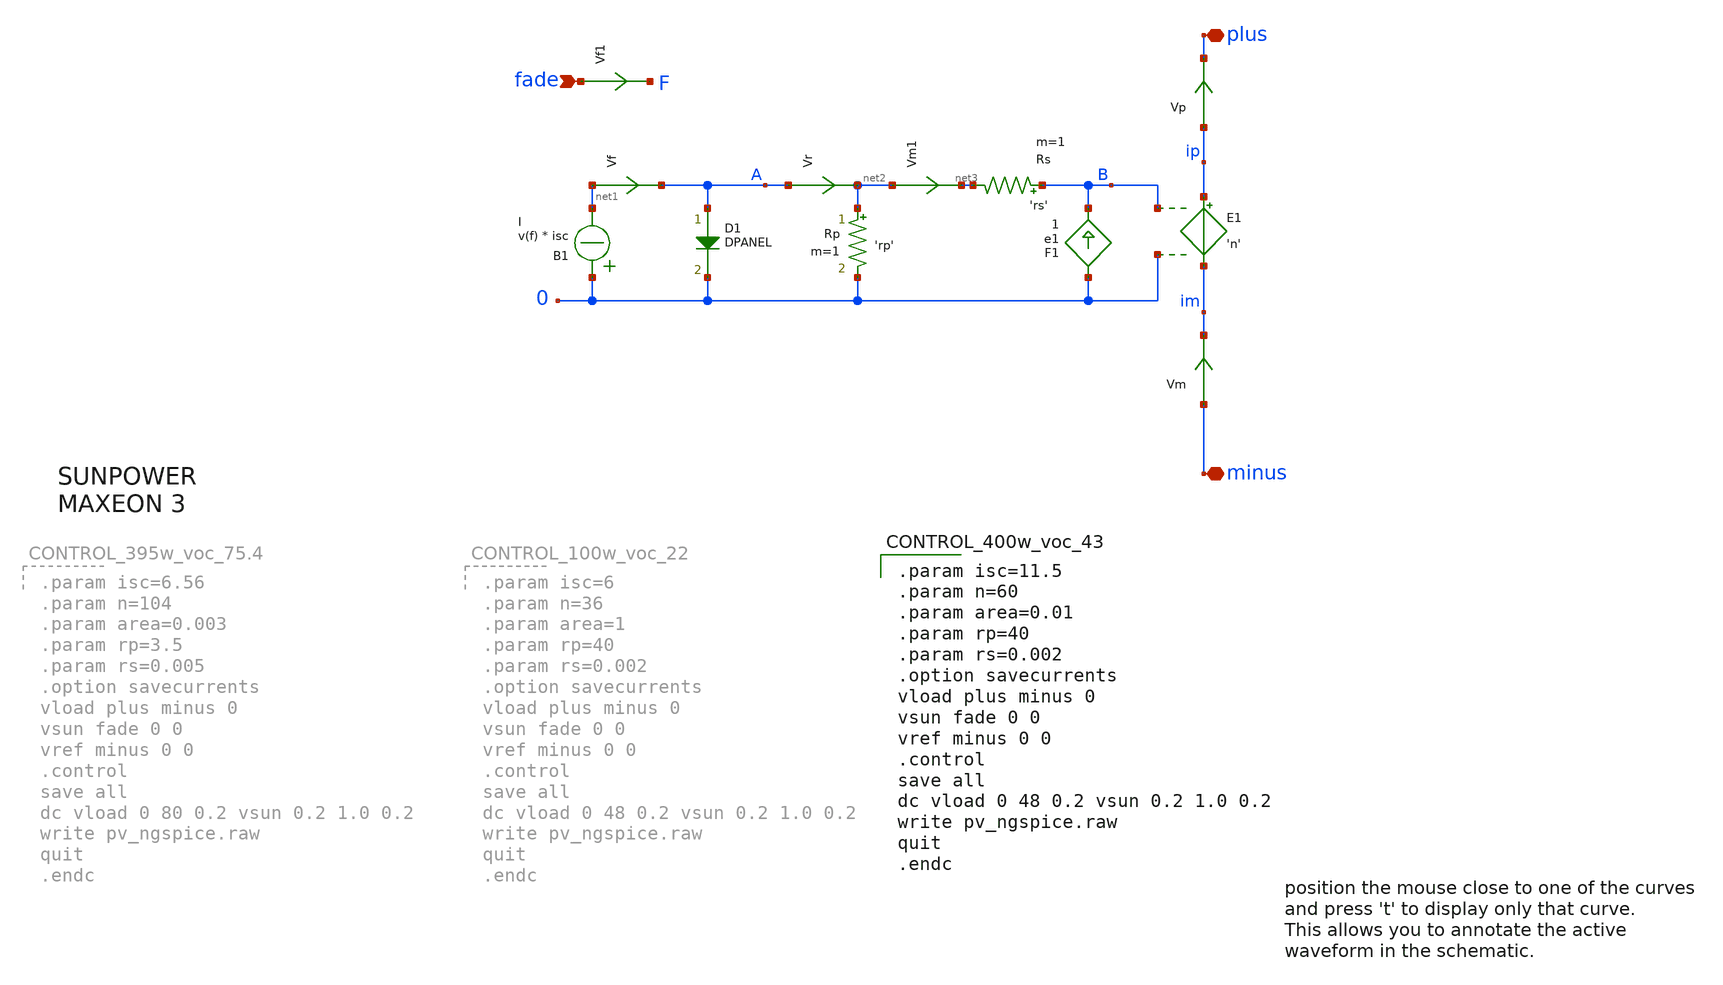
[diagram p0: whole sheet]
** sch_path: xschem_libraries_oa/ngspice/pv_ngspice/schematic/pv_ngspice.sch
* Copyright (C) 1998-2024 Stefan Frederik Schippers
* This program is free software; you can redistribute it and/or modify
* it under the terms of the GNU General Public License as published by
* the Free Software Foundation; either version 2 of the License, or
* (at your option) any later version.
* This program is distributed in the hope that it will be useful,
* but WITHOUT ANY WARRANTY; without even the implied warranty of
* MERCHANTABILITY or FITNESS FOR A PARTICULAR PURPOSE.  See the
* GNU General Public License for more details.
* You should have received a copy of the GNU General Public License
* along with this program; if not, write to the Free Software
**.subckt pv_ngspice minus fade plus
*.iopin minus
*.ipin fade
*.iopin plus
Vf net1 A 0
.save i(vf)
Vm minus im 0
.save i(vm)
Vp ip plus 0
.save i(vp)
D1 A 0 DPANEL area='area'
Rp net2 0 'rp' m=1
Rs B net3 'rs' m=1
F1 0 B e1 1
E1 ip im B 0 'n'
Vf1 fade F 0
.save i(vf1)
B1 0 net1 I = v(f) * isc
Vr A net2 0
.save i(vr)
Vm1 net2 net3 0
.save i(vm1)
**** begin user architecture code

.param isc=11.5
.param n=60
.param area=0.01
.param rp=40
.param rs=0.002
.option savecurrents
vload plus minus 0
vsun fade 0 0
vref minus 0 0
.control
save all
dc vload 0 48 0.2 vsun 0.2 1.0 0.2
write pv_ngspice.raw
quit
.endc


**** end user architecture code
**.ends
**** begin user architecture code
.model DPANEL D IS=1n N=1
**** end user architecture code
.end
